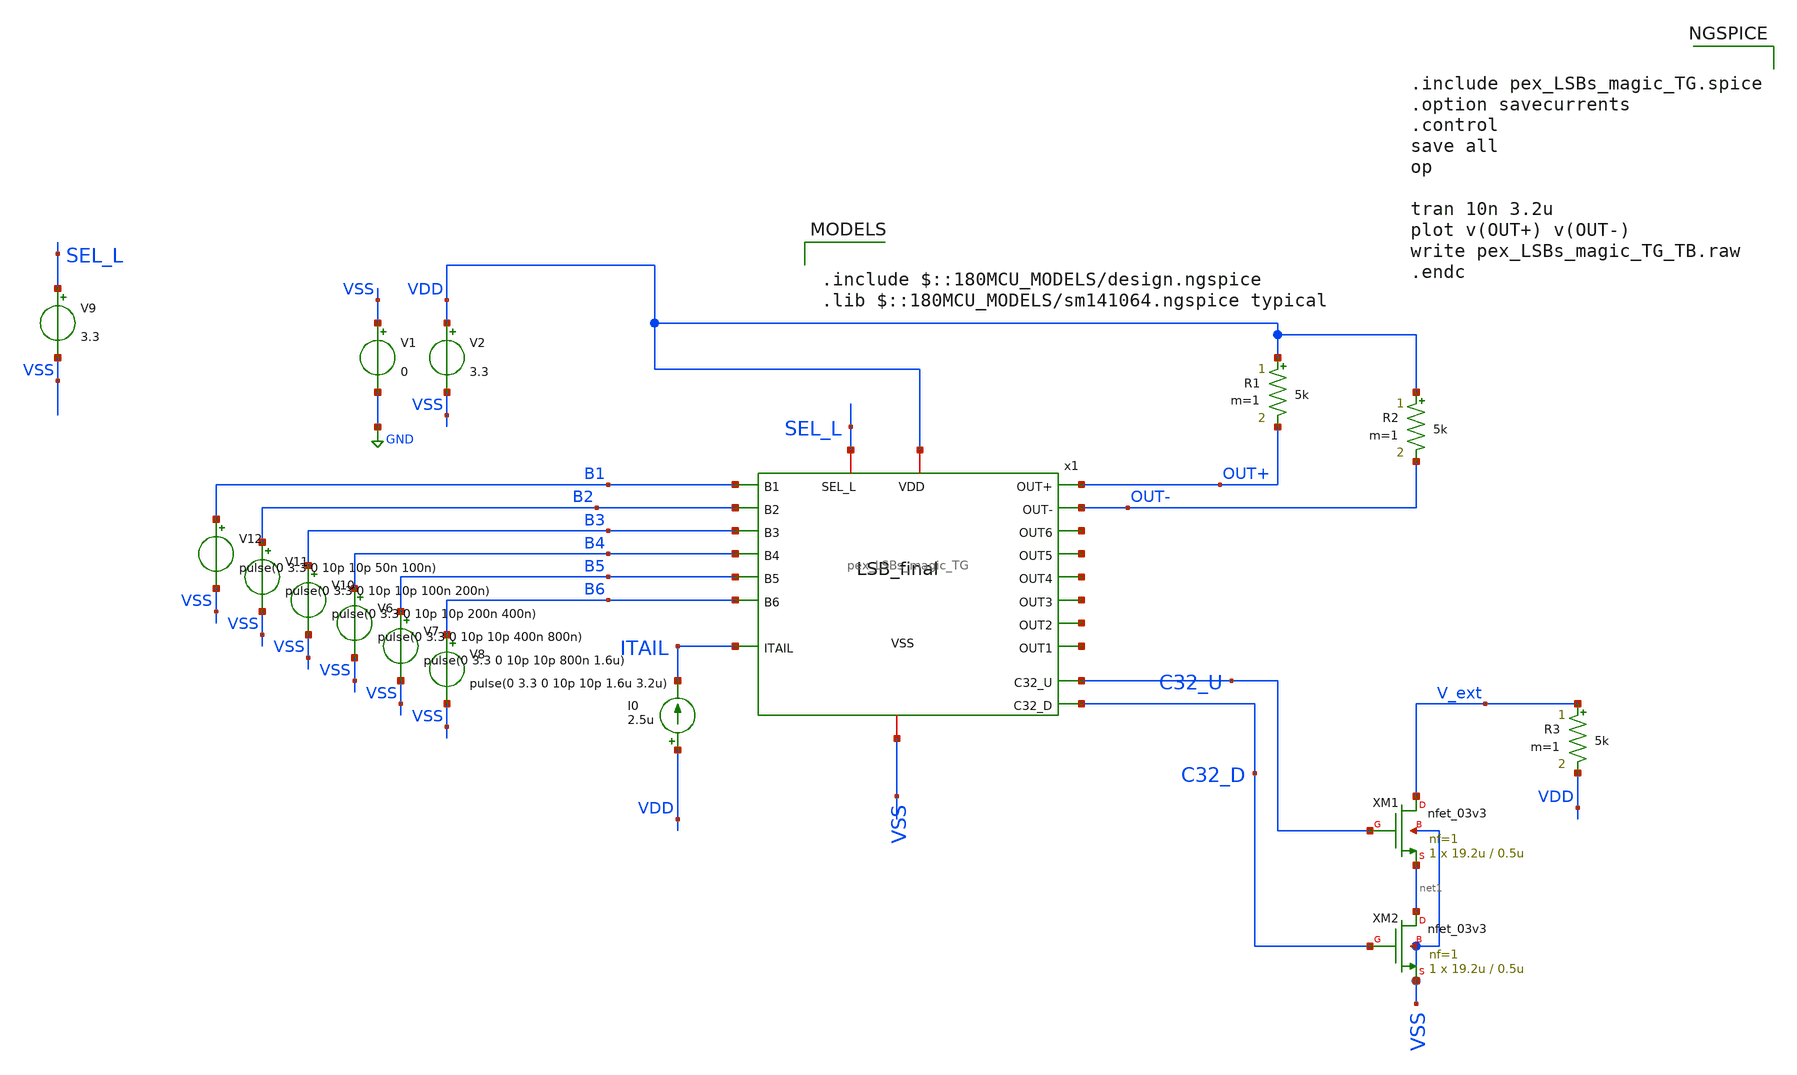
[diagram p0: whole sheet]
** sch_path: DAC_PAKISTAN_01/Pakistan1_Xschem/pex_LSBs_magic_TG_TB.sch
**.subckt pex_LSBs_magic_TG_TB
V1 VSS GND 0
V2 VDD VSS 3.3
V6 B4 VSS pulse(0 3.3 0 10p 10p 400n 800n)
V7 B5 VSS pulse(0 3.3 0 10p 10p 800n 1.6u)
V8 B6 VSS pulse(0 3.3 0 10p 10p 1.6u 3.2u)
V10 B3 VSS pulse(0 3.3 0 10p 10p 200n 400n)
V11 B2 VSS pulse(0 3.3 0 10p 10p 100n 200n)
V12 B1 VSS pulse(0 3.3 0 10p 10p 50n 100n)
I0 VDD ITAIL 2.5u
R1 VDD OUT+ 5k m=1
R2 VDD OUT- 5k m=1
V9 SEL_L VSS 3.3
x1 VDD VSS B1 B2 B3 B4 B5 B6 ITAIL OUT+ OUT- net2 net3 net4 net5 net6 net7 SEL_L C32_D C32_U
+ pex_LSBs_magic_TG
XM1 V_ext C32_U net1 VSS nfet_03v3 L=0.5u W=19.2u nf=1 ad='int((nf+1)/2) * W/nf * 0.18u' as='int((nf+2)/2) * W/nf * 0.18u'
+ pd='2*int((nf+1)/2) * (W/nf + 0.18u)' ps='2*int((nf+2)/2) * (W/nf + 0.18u)' nrd='0.18u / W' nrs='0.18u / W'
+ sa=0 sb=0 sd=0 m=1
XM2 net1 C32_D VSS VSS nfet_03v3 L=0.5u W=19.2u nf=1 ad='int((nf+1)/2) * W/nf * 0.18u' as='int((nf+2)/2) * W/nf * 0.18u'
+ pd='2*int((nf+1)/2) * (W/nf + 0.18u)' ps='2*int((nf+2)/2) * (W/nf + 0.18u)' nrd='0.18u / W' nrs='0.18u / W'
+ sa=0 sb=0 sd=0 m=1
R3 V_ext VDD 5k m=1
**** begin user architecture code

.include $::180MCU_MODELS/design.ngspice
.lib $::180MCU_MODELS/sm141064.ngspice typical



.include pex_LSBs_magic_TG.spice
.option savecurrents
.control
save all
op

tran 10n 3.2u
plot v(OUT+) v(OUT-)
write pex_LSBs_magic_TG_TB.raw
.endc


**** end user architecture code
**.ends
.GLOBAL GND
.end
